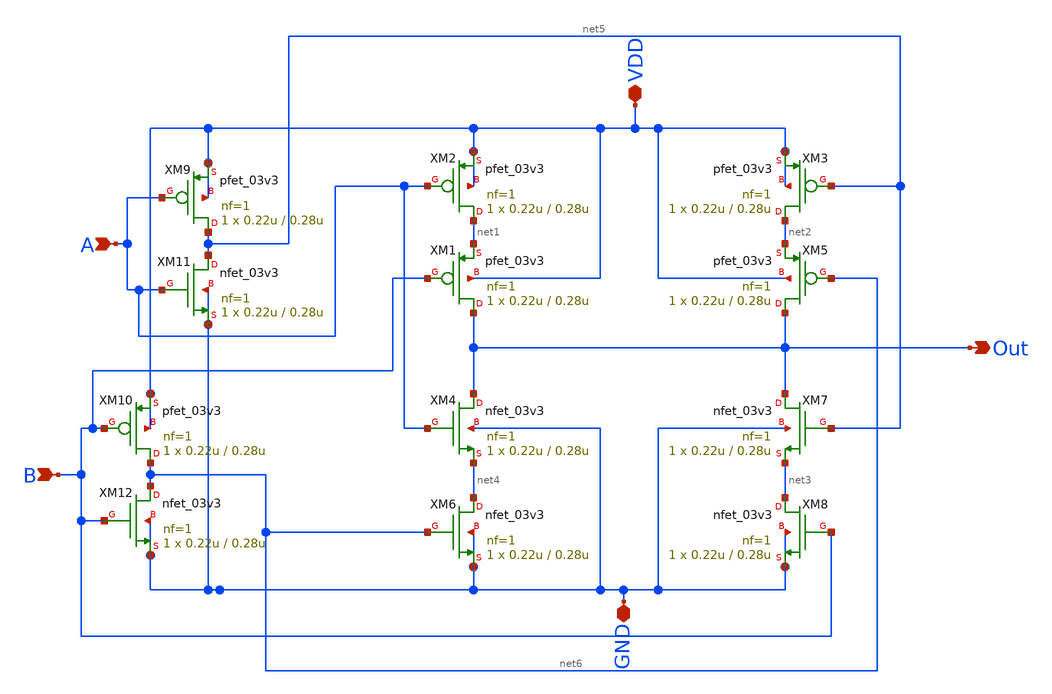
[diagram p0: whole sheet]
** sch_path: 2bit_Comparator/2x_drive/my_nxor.sch
**.subckt my_nxor VDD GND A B Out
*.iopin VDD
*.iopin GND
*.ipin A
*.ipin B
*.opin Out
XM2 net1 A VDD VDD pfet_03v3 L=0.28u W=0.22u nf=1 ad='int((nf+1)/2) * W/nf * 0.18u' as='int((nf+2)/2) * W/nf * 0.18u'
+ pd='2*int((nf+1)/2) * (W/nf + 0.18u)' ps='2*int((nf+2)/2) * (W/nf + 0.18u)' nrd='0.18u / W' nrs='0.18u / W'
+ sa=0 sb=0 sd=0 m=1
XM4 Out A net4 GND nfet_03v3 L=0.28u W=0.22u nf=1 ad='int((nf+1)/2) * W/nf * 0.18u' as='int((nf+2)/2) * W/nf * 0.18u'
+ pd='2*int((nf+1)/2) * (W/nf + 0.18u)' ps='2*int((nf+2)/2) * (W/nf + 0.18u)' nrd='0.18u / W' nrs='0.18u / W'
+ sa=0 sb=0 sd=0 m=1
XM1 Out B net1 VDD pfet_03v3 L=0.28u W=0.22u nf=1 ad='int((nf+1)/2) * W/nf * 0.18u' as='int((nf+2)/2) * W/nf * 0.18u'
+ pd='2*int((nf+1)/2) * (W/nf + 0.18u)' ps='2*int((nf+2)/2) * (W/nf + 0.18u)' nrd='0.18u / W' nrs='0.18u / W'
+ sa=0 sb=0 sd=0 m=1
XM3 net2 net5 VDD VDD pfet_03v3 L=0.28u W=0.22u nf=1 ad='int((nf+1)/2) * W/nf * 0.18u' as='int((nf+2)/2) * W/nf * 0.18u'
+ pd='2*int((nf+1)/2) * (W/nf + 0.18u)' ps='2*int((nf+2)/2) * (W/nf + 0.18u)' nrd='0.18u / W' nrs='0.18u / W'
+ sa=0 sb=0 sd=0 m=1
XM5 Out net6 net2 VDD pfet_03v3 L=0.28u W=0.22u nf=1 ad='int((nf+1)/2) * W/nf * 0.18u' as='int((nf+2)/2) * W/nf * 0.18u'
+ pd='2*int((nf+1)/2) * (W/nf + 0.18u)' ps='2*int((nf+2)/2) * (W/nf + 0.18u)' nrd='0.18u / W' nrs='0.18u / W'
+ sa=0 sb=0 sd=0 m=1
XM6 net4 net6 GND GND nfet_03v3 L=0.28u W=0.22u nf=1 ad='int((nf+1)/2) * W/nf * 0.18u' as='int((nf+2)/2) * W/nf * 0.18u'
+ pd='2*int((nf+1)/2) * (W/nf + 0.18u)' ps='2*int((nf+2)/2) * (W/nf + 0.18u)' nrd='0.18u / W' nrs='0.18u / W'
+ sa=0 sb=0 sd=0 m=1
XM7 Out net5 net3 GND nfet_03v3 L=0.28u W=0.22u nf=1 ad='int((nf+1)/2) * W/nf * 0.18u' as='int((nf+2)/2) * W/nf * 0.18u'
+ pd='2*int((nf+1)/2) * (W/nf + 0.18u)' ps='2*int((nf+2)/2) * (W/nf + 0.18u)' nrd='0.18u / W' nrs='0.18u / W'
+ sa=0 sb=0 sd=0 m=1
XM8 net3 B GND GND nfet_03v3 L=0.28u W=0.22u nf=1 ad='int((nf+1)/2) * W/nf * 0.18u' as='int((nf+2)/2) * W/nf * 0.18u'
+ pd='2*int((nf+1)/2) * (W/nf + 0.18u)' ps='2*int((nf+2)/2) * (W/nf + 0.18u)' nrd='0.18u / W' nrs='0.18u / W'
+ sa=0 sb=0 sd=0 m=1
XM9 net5 A VDD VDD pfet_03v3 L=0.28u W=0.22u nf=1 ad='int((nf+1)/2) * W/nf * 0.18u' as='int((nf+2)/2) * W/nf * 0.18u'
+ pd='2*int((nf+1)/2) * (W/nf + 0.18u)' ps='2*int((nf+2)/2) * (W/nf + 0.18u)' nrd='0.18u / W' nrs='0.18u / W'
+ sa=0 sb=0 sd=0 m=1
XM10 net6 B VDD VDD pfet_03v3 L=0.28u W=0.22u nf=1 ad='int((nf+1)/2) * W/nf * 0.18u' as='int((nf+2)/2) * W/nf * 0.18u'
+ pd='2*int((nf+1)/2) * (W/nf + 0.18u)' ps='2*int((nf+2)/2) * (W/nf + 0.18u)' nrd='0.18u / W' nrs='0.18u / W'
+ sa=0 sb=0 sd=0 m=1
XM11 net5 A GND GND nfet_03v3 L=0.28u W=0.22u nf=1 ad='int((nf+1)/2) * W/nf * 0.18u' as='int((nf+2)/2) * W/nf * 0.18u'
+ pd='2*int((nf+1)/2) * (W/nf + 0.18u)' ps='2*int((nf+2)/2) * (W/nf + 0.18u)' nrd='0.18u / W' nrs='0.18u / W'
+ sa=0 sb=0 sd=0 m=1
XM12 net6 B GND GND nfet_03v3 L=0.28u W=0.22u nf=1 ad='int((nf+1)/2) * W/nf * 0.18u' as='int((nf+2)/2) * W/nf * 0.18u'
+ pd='2*int((nf+1)/2) * (W/nf + 0.18u)' ps='2*int((nf+2)/2) * (W/nf + 0.18u)' nrd='0.18u / W' nrs='0.18u / W'
+ sa=0 sb=0 sd=0 m=1
**.ends
.end
